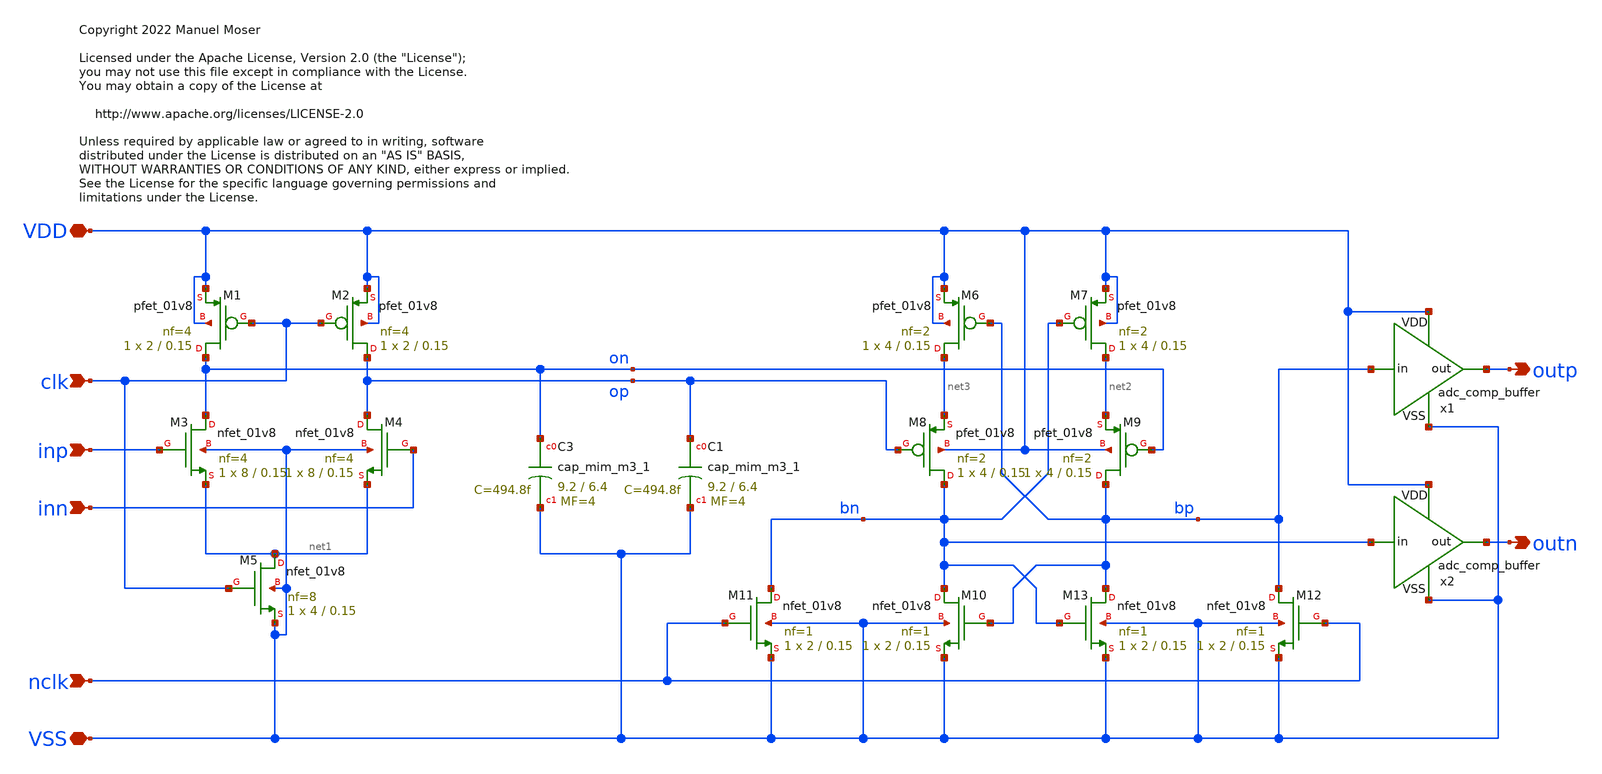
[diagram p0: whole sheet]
** sch_path: xschem/adc_comp_circuit/adc_comp_circuit.sch
* Copyright 2022 Manuel Moser
* Licensed under the Apache License, Version 2.0 (the "License");
**.subckt adc_comp_circuit VDD VSS inp inn clk nclk outp outn
*.iopin VDD
*.iopin VSS
*.ipin inp
*.ipin inn
*.ipin clk
*.ipin nclk
*.opin outp
*.opin outn
XM1 on clk VDD VDD sky130_fd_pr__pfet_01v8 L=0.15 W=2 nf=4 ad='int((nf+1)/2) * W/nf * 0.29' as='int((nf+2)/2) * W/nf * 0.29'
+ pd='2*int((nf+1)/2) * (W/nf + 0.29)' ps='2*int((nf+2)/2) * (W/nf + 0.29)' nrd='0.29 / W' nrs='0.29 / W'
+ sa=0 sb=0 sd=0 mult=1 m=1
XM2 op clk VDD VDD sky130_fd_pr__pfet_01v8 L=0.15 W=2 nf=4 ad='int((nf+1)/2) * W/nf * 0.29' as='int((nf+2)/2) * W/nf * 0.29'
+ pd='2*int((nf+1)/2) * (W/nf + 0.29)' ps='2*int((nf+2)/2) * (W/nf + 0.29)' nrd='0.29 / W' nrs='0.29 / W'
+ sa=0 sb=0 sd=0 mult=1 m=1
XM3 on inp net1 VSS sky130_fd_pr__nfet_01v8 L=0.15 W=8 nf=4 ad='int((nf+1)/2) * W/nf * 0.29' as='int((nf+2)/2) * W/nf * 0.29'
+ pd='2*int((nf+1)/2) * (W/nf + 0.29)' ps='2*int((nf+2)/2) * (W/nf + 0.29)' nrd='0.29 / W' nrs='0.29 / W'
+ sa=0 sb=0 sd=0 mult=1 m=1
XM4 op inn net1 VSS sky130_fd_pr__nfet_01v8 L=0.15 W=8 nf=4 ad='int((nf+1)/2) * W/nf * 0.29' as='int((nf+2)/2) * W/nf * 0.29'
+ pd='2*int((nf+1)/2) * (W/nf + 0.29)' ps='2*int((nf+2)/2) * (W/nf + 0.29)' nrd='0.29 / W' nrs='0.29 / W'
+ sa=0 sb=0 sd=0 mult=1 m=1
XM5 net1 clk VSS VSS sky130_fd_pr__nfet_01v8 L=0.15 W=4 nf=8 ad='int((nf+1)/2) * W/nf * 0.29' as='int((nf+2)/2) * W/nf * 0.29'
+ pd='2*int((nf+1)/2) * (W/nf + 0.29)' ps='2*int((nf+2)/2) * (W/nf + 0.29)' nrd='0.29 / W' nrs='0.29 / W'
+ sa=0 sb=0 sd=0 mult=1 m=1
XM6 net3 bp VDD VDD sky130_fd_pr__pfet_01v8 L=0.15 W=4 nf=2 ad='int((nf+1)/2) * W/nf * 0.29' as='int((nf+2)/2) * W/nf * 0.29'
+ pd='2*int((nf+1)/2) * (W/nf + 0.29)' ps='2*int((nf+2)/2) * (W/nf + 0.29)' nrd='0.29 / W' nrs='0.29 / W'
+ sa=0 sb=0 sd=0 mult=1 m=1
XM7 net2 bn VDD VDD sky130_fd_pr__pfet_01v8 L=0.15 W=4 nf=2 ad='int((nf+1)/2) * W/nf * 0.29' as='int((nf+2)/2) * W/nf * 0.29'
+ pd='2*int((nf+1)/2) * (W/nf + 0.29)' ps='2*int((nf+2)/2) * (W/nf + 0.29)' nrd='0.29 / W' nrs='0.29 / W'
+ sa=0 sb=0 sd=0 mult=1 m=1
XM8 bn op net3 VDD sky130_fd_pr__pfet_01v8 L=0.15 W=4 nf=2 ad='int((nf+1)/2) * W/nf * 0.29' as='int((nf+2)/2) * W/nf * 0.29'
+ pd='2*int((nf+1)/2) * (W/nf + 0.29)' ps='2*int((nf+2)/2) * (W/nf + 0.29)' nrd='0.29 / W' nrs='0.29 / W'
+ sa=0 sb=0 sd=0 mult=1 m=1
XM9 bp on net2 VDD sky130_fd_pr__pfet_01v8 L=0.15 W=4 nf=2 ad='int((nf+1)/2) * W/nf * 0.29' as='int((nf+2)/2) * W/nf * 0.29'
+ pd='2*int((nf+1)/2) * (W/nf + 0.29)' ps='2*int((nf+2)/2) * (W/nf + 0.29)' nrd='0.29 / W' nrs='0.29 / W'
+ sa=0 sb=0 sd=0 mult=1 m=1
XM10 bn bp VSS VSS sky130_fd_pr__nfet_01v8 L=0.15 W=2 nf=1 ad='int((nf+1)/2) * W/nf * 0.29' as='int((nf+2)/2) * W/nf * 0.29'
+ pd='2*int((nf+1)/2) * (W/nf + 0.29)' ps='2*int((nf+2)/2) * (W/nf + 0.29)' nrd='0.29 / W' nrs='0.29 / W'
+ sa=0 sb=0 sd=0 mult=1 m=1
XM11 bn nclk VSS VSS sky130_fd_pr__nfet_01v8 L=0.15 W=2 nf=1 ad='int((nf+1)/2) * W/nf * 0.29' as='int((nf+2)/2) * W/nf * 0.29'
+ pd='2*int((nf+1)/2) * (W/nf + 0.29)' ps='2*int((nf+2)/2) * (W/nf + 0.29)' nrd='0.29 / W' nrs='0.29 / W'
+ sa=0 sb=0 sd=0 mult=1 m=1
XM12 bp nclk VSS VSS sky130_fd_pr__nfet_01v8 L=0.15 W=2 nf=1 ad='int((nf+1)/2) * W/nf * 0.29' as='int((nf+2)/2) * W/nf * 0.29'
+ pd='2*int((nf+1)/2) * (W/nf + 0.29)' ps='2*int((nf+2)/2) * (W/nf + 0.29)' nrd='0.29 / W' nrs='0.29 / W'
+ sa=0 sb=0 sd=0 mult=1 m=1
XM13 bp bn VSS VSS sky130_fd_pr__nfet_01v8 L=0.15 W=2 nf=1 ad='int((nf+1)/2) * W/nf * 0.29' as='int((nf+2)/2) * W/nf * 0.29'
+ pd='2*int((nf+1)/2) * (W/nf + 0.29)' ps='2*int((nf+2)/2) * (W/nf + 0.29)' nrd='0.29 / W' nrs='0.29 / W'
+ sa=0 sb=0 sd=0 mult=1 m=1
x1 VDD VSS bp outp adc_comp_buffer
x2 VDD VSS bn outn adc_comp_buffer
XC3 on VSS sky130_fd_pr__cap_mim_m3_1 W=9.2 L=6.4 MF=4 m=4
XC1 op VSS sky130_fd_pr__cap_mim_m3_1 W=9.2 L=6.4 MF=4 m=4
**.ends

* expanding   symbol:  /foss/designs/SKY130_SAR-ADC/xschem/adc_comp_buffer/adc_comp_buffer.sym # of
*+ pins=4
** sym_path: xschem/adc_comp_buffer.sym
** sch_path: xschem/adc_comp_buffer.sch
.subckt adc_comp_buffer VDD VSS in out
*.iopin VDD
*.iopin VSS
*.ipin in
*.opin out
XM5 net1 in VSS VSS sky130_fd_pr__nfet_01v8 L=0.15 W=0.5 nf=1 ad='int((nf+1)/2) * W/nf * 0.29' as='int((nf+2)/2) * W/nf * 0.29'
+ pd='2*int((nf+1)/2) * (W/nf + 0.29)' ps='2*int((nf+2)/2) * (W/nf + 0.29)' nrd='0.29 / W' nrs='0.29 / W'
+ sa=0 sb=0 sd=0 mult=1 m=1
XM1 net1 in VDD VDD sky130_fd_pr__pfet_01v8 L=0.15 W=1 nf=1 ad='int((nf+1)/2) * W/nf * 0.29' as='int((nf+2)/2) * W/nf * 0.29'
+ pd='2*int((nf+1)/2) * (W/nf + 0.29)' ps='2*int((nf+2)/2) * (W/nf + 0.29)' nrd='0.29 / W' nrs='0.29 / W'
+ sa=0 sb=0 sd=0 mult=1 m=1
XM2 out net1 VDD VDD sky130_fd_pr__pfet_01v8 L=0.15 W=2 nf=2 ad='int((nf+1)/2) * W/nf * 0.29' as='int((nf+2)/2) * W/nf * 0.29'
+ pd='2*int((nf+1)/2) * (W/nf + 0.29)' ps='2*int((nf+2)/2) * (W/nf + 0.29)' nrd='0.29 / W' nrs='0.29 / W'
+ sa=0 sb=0 sd=0 mult=1 m=1
XM6 out net1 VSS VSS sky130_fd_pr__nfet_01v8 L=0.15 W=1 nf=2 ad='int((nf+1)/2) * W/nf * 0.29' as='int((nf+2)/2) * W/nf * 0.29'
+ pd='2*int((nf+1)/2) * (W/nf + 0.29)' ps='2*int((nf+2)/2) * (W/nf + 0.29)' nrd='0.29 / W' nrs='0.29 / W'
+ sa=0 sb=0 sd=0 mult=1 m=1
.ends

.end
